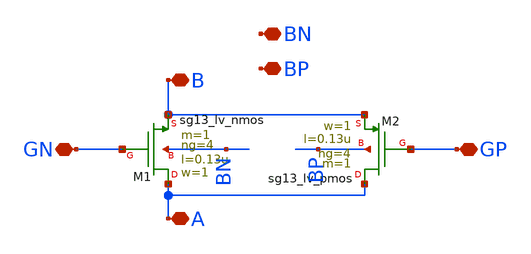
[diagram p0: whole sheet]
** sch_path: DelayLine/others/transmission_gate.sch
**.subckt transmission_gate B GN A GP BN BP
*.iopin B
*.iopin GN
*.iopin A
*.iopin GP
*.iopin BN
*.iopin BP
XM1 A GN B BN sg13_lv_nmos w=1 l=0.13u ng=4 m=1 mm_ok=1
XM2 A GP B BP sg13_lv_pmos w=1 l=0.13u ng=4 m=1 mm_ok=1
**.ends
.end
